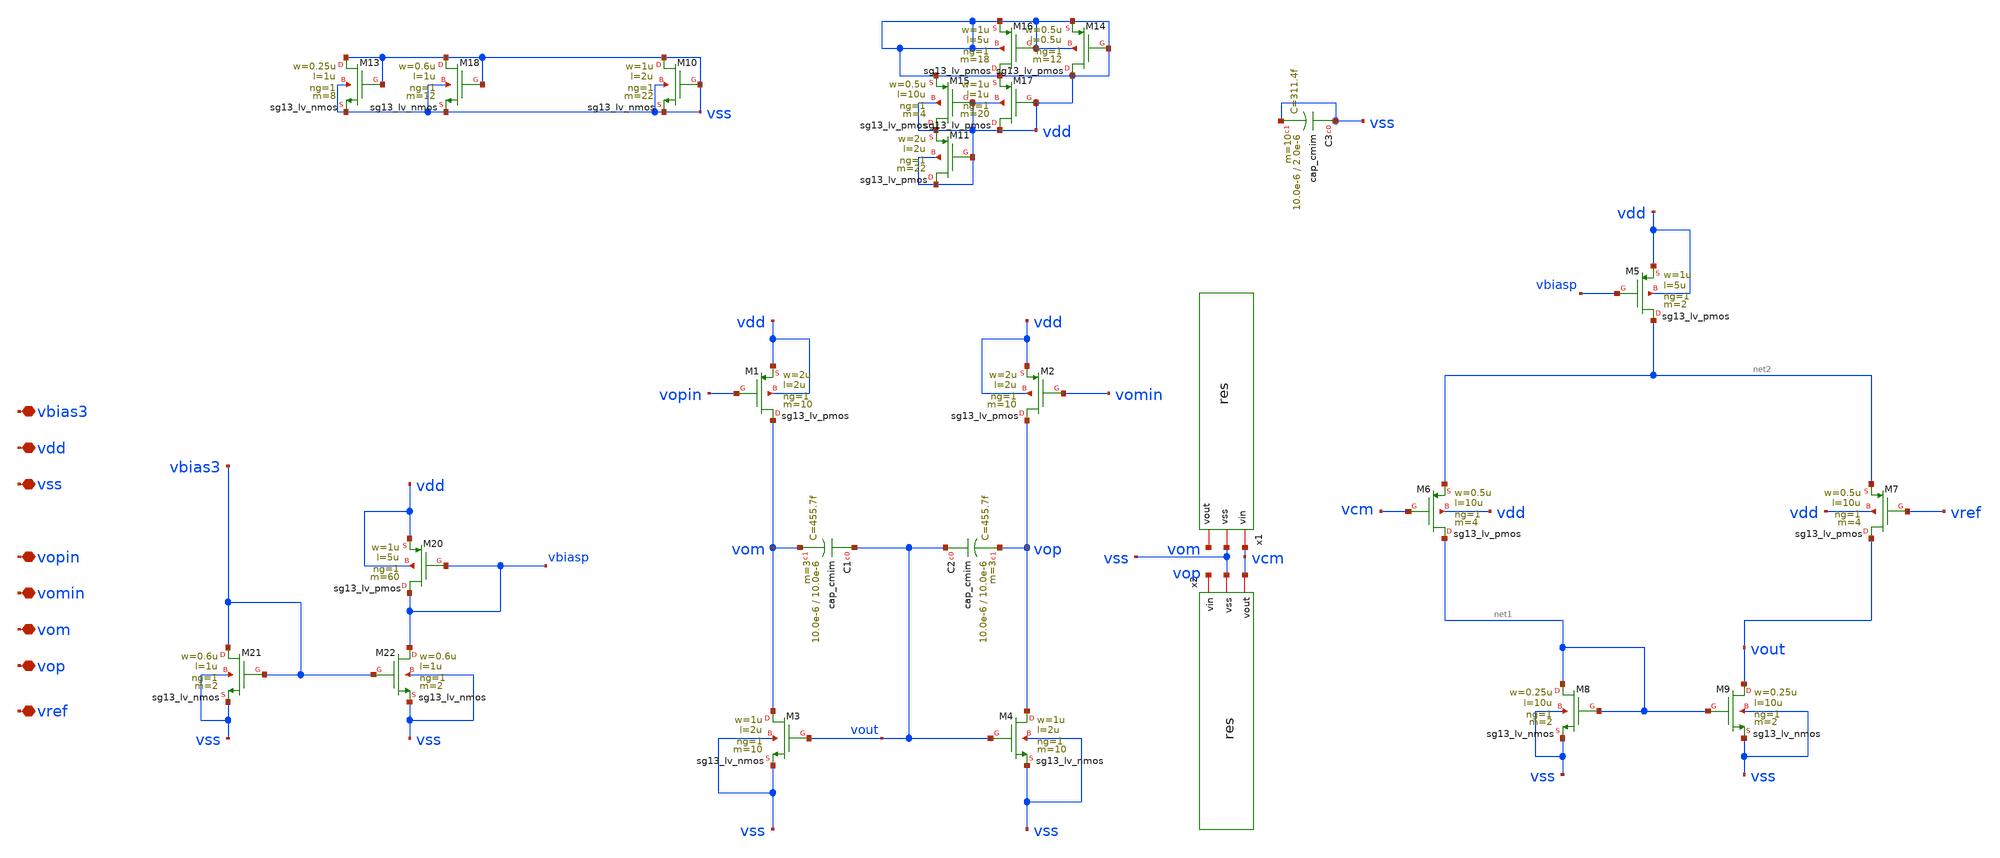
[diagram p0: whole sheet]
** sch_path: LVS/Unic_cass_final_design_lvs/Simulations/Opamp_design/Src/common_source_stage.sch
**.subckt common_source_stage vbias3 vdd vss vopin vomin vom vop vref
*.iopin vbias3
*.iopin vdd
*.iopin vss
*.iopin vopin
*.iopin vomin
*.iopin vom
*.iopin vop
*.iopin vref
XM20 vbiasp vbiasp vdd vdd sg13_lv_pmos w=1u l=5u ng=1 m=60 mm_ok=1
XM21 vbias3 vbias3 vss vss sg13_lv_nmos w=0.6u l=1u ng=1 m=2 mm_ok=1
XM22 vbiasp vbias3 vss vss sg13_lv_nmos w=0.6u l=1u ng=1 m=2 mm_ok=1
XM1 vom vopin vdd vdd sg13_lv_pmos w=2u l=2u ng=1 m=10 mm_ok=1
XM2 vop vomin vdd vdd sg13_lv_pmos w=2u l=2u ng=1 m=10 mm_ok=1
XM3 vom vout vss vss sg13_lv_nmos w=1u l=2u ng=1 m=10 mm_ok=1
XM4 vop vout vss vss sg13_lv_nmos w=1u l=2u ng=1 m=10 mm_ok=1
XM5 net2 vbiasp vdd vdd sg13_lv_pmos w=1u l=5u ng=1 m=2 mm_ok=1
XM6 net1 vcm net2 vdd sg13_lv_pmos w=0.5u l=10u ng=1 m=4 mm_ok=1
XM7 vout vref net2 vdd sg13_lv_pmos w=0.5u l=10u ng=1 m=4 mm_ok=1
XM8 net1 net1 vss vss sg13_lv_nmos w=0.25u l=10u ng=1 m=2 mm_ok=1
XM9 vout net1 vss vss sg13_lv_nmos w=0.25u l=10u ng=1 m=2 mm_ok=1
XC1 vout vom cap_cmim w=10.0e-6 l=10.0e-6 m=3 mm_ok=1
XC2 vout vop cap_cmim w=10.0e-6 l=10.0e-6 m=3 mm_ok=1
XM10 vss vss vss vss sg13_lv_nmos w=1u l=2u ng=1 m=22 mm_ok=1
XM13 vss vss vss vss sg13_lv_nmos w=0.25u l=1u ng=1 m=8 mm_ok=1
XM14 vdd vdd vdd vdd sg13_lv_pmos w=0.5u l=0.5u ng=1 m=12 mm_ok=1
XM15 vdd vdd vdd vdd sg13_lv_pmos w=0.5u l=10u ng=1 m=4 mm_ok=1
XM17 vdd vdd vdd vdd sg13_lv_pmos w=1u l=1u ng=1 m=20 mm_ok=1
XM18 vss vss vss vss sg13_lv_nmos w=0.6u l=1u ng=1 m=12 mm_ok=1
XM16 vdd vdd vdd vdd sg13_lv_pmos w=1u l=5u ng=1 m=18 mm_ok=1
XM11 vdd vdd vdd vdd sg13_lv_pmos w=2u l=2u ng=1 m=22 mm_ok=1
XC3 vss vss cap_cmim w=10.0e-6 l=2.0e-6 m=10 mm_ok=1
x1 vcm vss vom res
x2 vop vss vcm res
**.ends

* expanding   symbol:
*+  /home/designer/shared/Unic_Cass_IHP/LVS/Unic_cass_final_design_lvs/Simulations/Opamp_design/Src/res.sym # of pins=3
** sym_path: LVS/Unic_cass_final_design_lvs/Simulations/Opamp_design/Src/res.sym
** sch_path: LVS/Unic_cass_final_design_lvs/Simulations/Opamp_design/Src/res.sch
.subckt res vin vss vout
*.iopin vin
*.iopin vout
*.iopin vss
XR21 vin net4 vss rhigh w=0.5e-6 l=1e-6 m=1 b=0 mm_ok=1
XR1 net4 net5 vss rhigh w=0.5e-6 l=1e-6 m=1 b=0 mm_ok=1
XR2 net5 net6 vss rhigh w=0.5e-6 l=1e-6 m=1 b=0 mm_ok=1
XR3 net6 net7 vss rhigh w=0.5e-6 l=1e-6 m=1 b=0 mm_ok=1
XR4 net7 net1 vss rhigh w=0.5e-6 l=1e-6 m=1 b=0 mm_ok=1
XR5 net2 net8 vss rhigh w=0.5e-6 l=1e-6 m=1 b=0 mm_ok=1
XR6 net8 net9 vss rhigh w=0.5e-6 l=1e-6 m=1 b=0 mm_ok=1
XR7 net9 net10 vss rhigh w=0.5e-6 l=1e-6 m=1 b=0 mm_ok=1
XR8 net10 net11 vss rhigh w=0.5e-6 l=1e-6 m=1 b=0 mm_ok=1
XR9 net11 net1 vss rhigh w=0.5e-6 l=1e-6 m=1 b=0 mm_ok=1
XR10 net2 net12 vss rhigh w=0.5e-6 l=1e-6 m=1 b=0 mm_ok=1
XR11 net12 net13 vss rhigh w=0.5e-6 l=1e-6 m=1 b=0 mm_ok=1
XR12 net13 net14 vss rhigh w=0.5e-6 l=1e-6 m=1 b=0 mm_ok=1
XR13 net14 net15 vss rhigh w=0.5e-6 l=1e-6 m=1 b=0 mm_ok=1
XR14 net15 net3 vss rhigh w=0.5e-6 l=1e-6 m=1 b=0 mm_ok=1
XR15 vout net16 vss rhigh w=0.5e-6 l=1e-6 m=1 b=0 mm_ok=1
XR16 net16 net17 vss rhigh w=0.5e-6 l=1e-6 m=1 b=0 mm_ok=1
XR17 net17 net18 vss rhigh w=0.5e-6 l=1e-6 m=1 b=0 mm_ok=1
XR18 net18 net19 vss rhigh w=0.5e-6 l=1e-6 m=1 b=0 mm_ok=1
XR19 net19 net3 vss rhigh w=0.5e-6 l=1e-6 m=1 b=0 mm_ok=1
.ends

.end
